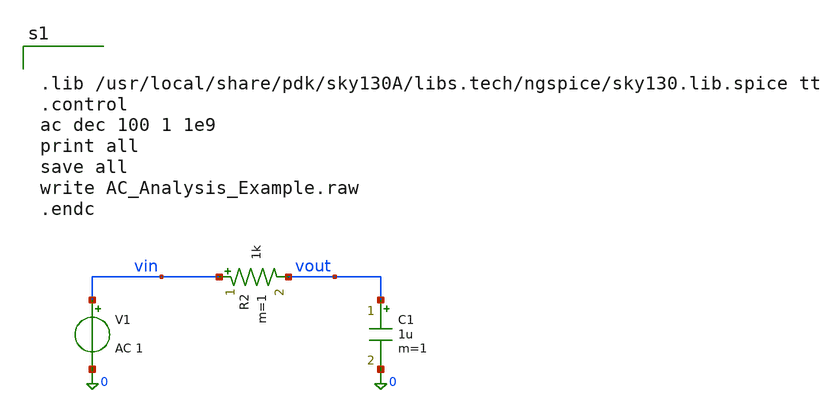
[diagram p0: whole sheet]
** sch_path: mag/layout/AC_Analysis_Example.sch
**.subckt AC_Analysis_Example
V1 vin 0 AC 1
R2 vin vout 1k m=1
C1 vout 0 1u m=1
**** begin user architecture code


.lib /usr/local/share/pdk/sky130A/libs.tech/ngspice/sky130.lib.spice tt
.control
ac dec 100 1 1e9
print all
save all
write AC_Analysis_Example.raw
.endc

**** end user architecture code
**.ends
.end
